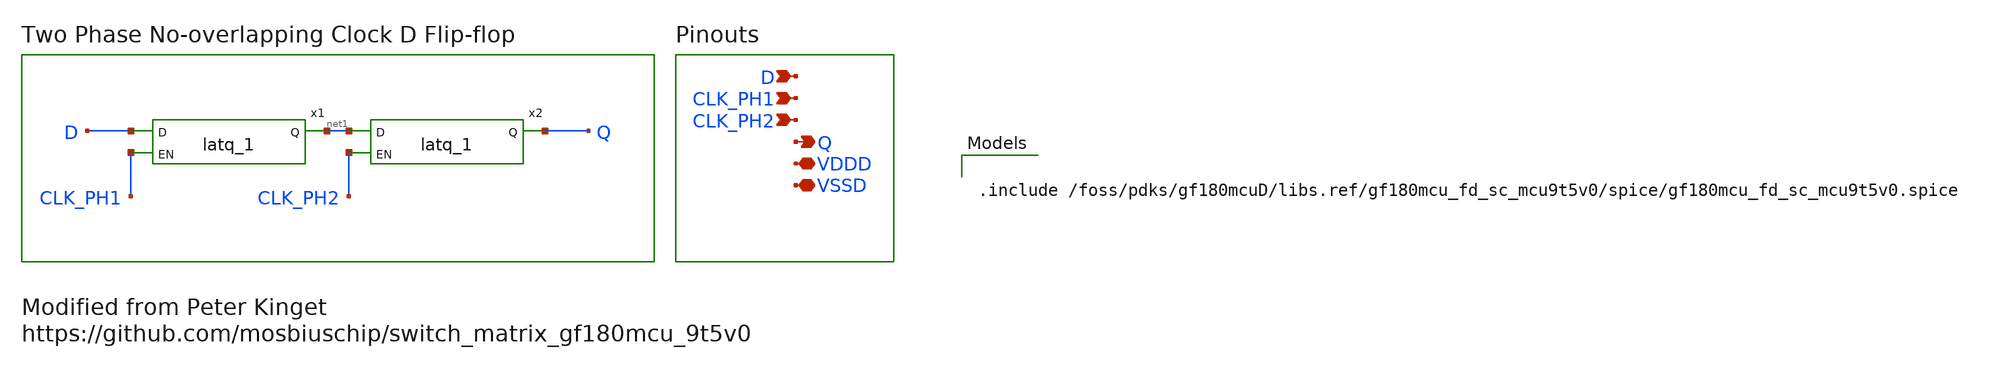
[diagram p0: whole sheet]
** sch_path: designs/libs/core_switch_matrix/dff_2ph_clk/dff_2ph_clk.sch
**.subckt dff_2ph_clk D CLK_PH1 CLK_PH2 Q VDDD VSSD
*.ipin D
*.ipin CLK_PH1
*.ipin CLK_PH2
*.opin Q
*.iopin VDDD
*.iopin VSSD
x1 D CLK_PH1 net1 VDDD VDDD VSSD VSSD gf180mcu_fd_sc_mcu9t5v0__latq_1
x2 net1 CLK_PH2 Q VDDD VDDD VSSD VSSD gf180mcu_fd_sc_mcu9t5v0__latq_1
**** begin user architecture code

.include /foss/pdks/gf180mcuD/libs.ref/gf180mcu_fd_sc_mcu9t5v0/spice/gf180mcu_fd_sc_mcu9t5v0.spice

**** end user architecture code
**.ends
.end
